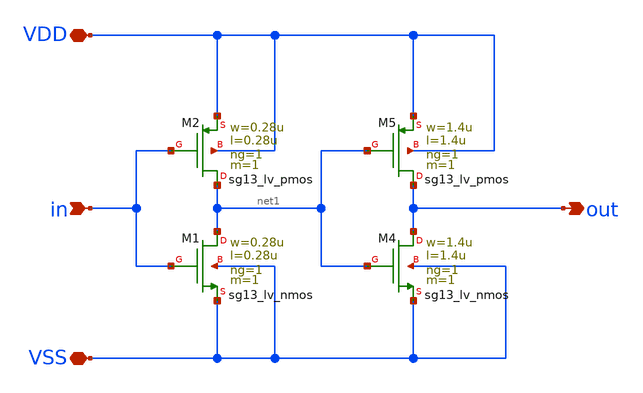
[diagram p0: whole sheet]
** sch_path: blocks/composite/dpi_adexp_neuron/design_data/xschem/buff.sch
**.subckt buff VDD in VSS out
*.iopin VDD
*.ipin in
*.iopin VSS
*.opin out
XM1 net1 in VSS VSS sg13_lv_nmos w=0.28u l=0.28u ng=1 m=1 mm_ok=1
XM2 net1 in VDD VDD sg13_lv_pmos w=0.28u l=0.28u ng=1 m=1 mm_ok=1
XM4 out net1 VSS VSS sg13_lv_nmos w=1.4u l=1.4u ng=1 m=1 mm_ok=1
XM5 out net1 VDD VDD sg13_lv_pmos w=1.4u l=1.4u ng=1 m=1 mm_ok=1
**.ends
.end
